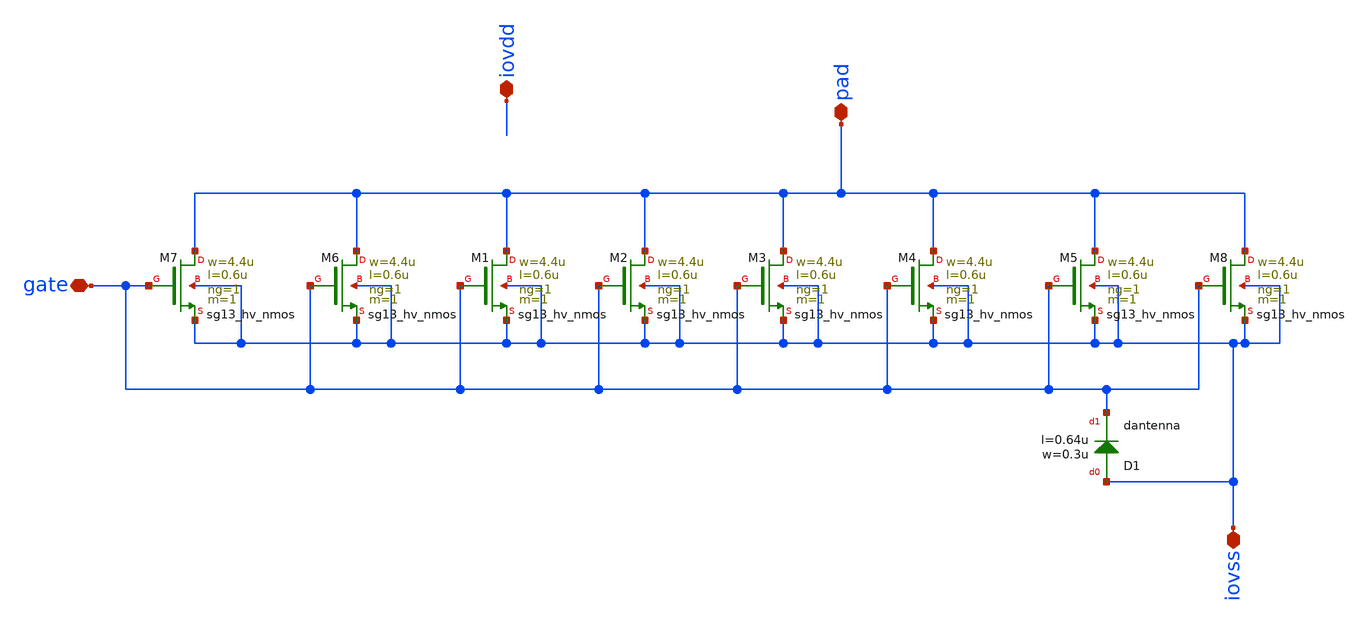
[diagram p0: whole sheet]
** sch_path: ihp-sg13g2/libs.ref/sg13g2_io/xschem/sg13g2_Clamp_N8N8D.sch
**.subckt sg13g2_Clamp_N8N8D iovss pad gate iovdd
*.iopin iovss
*.iopin pad
*.iopin gate
*.iopin iovdd
XM1 pad gate iovss iovss sg13_hv_nmos w=4.4u l=0.6u ng=1 m=1
XM2 pad gate iovss iovss sg13_hv_nmos w=4.4u l=0.6u ng=1 m=1
XM3 pad gate iovss iovss sg13_hv_nmos w=4.4u l=0.6u ng=1 m=1
XM4 pad gate iovss iovss sg13_hv_nmos w=4.4u l=0.6u ng=1 m=1
XM5 pad gate iovss iovss sg13_hv_nmos w=4.4u l=0.6u ng=1 m=1
XM6 pad gate iovss iovss sg13_hv_nmos w=4.4u l=0.6u ng=1 m=1
XM7 pad gate iovss iovss sg13_hv_nmos w=4.4u l=0.6u ng=1 m=1
XM8 pad gate iovss iovss sg13_hv_nmos w=4.4u l=0.6u ng=1 m=1
XD1 iovss gate dantenna l=0.64u w=0.3u
**.ends
.end
